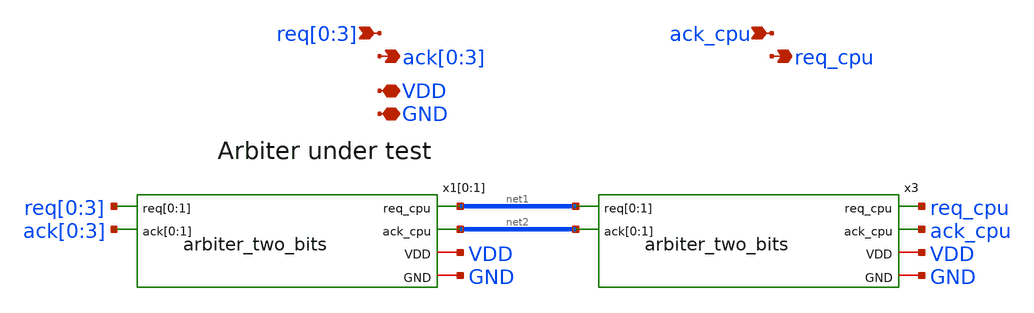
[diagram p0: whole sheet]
** sch_path: design/xschem/arbiter_tree_four_bits.sch
**.subckt arbiter_tree_four_bits req[0],req[1],req[2],req[3] ack[0],ack[1],ack[2],ack[3] ack_cpu
*+ req_cpu VDD GND
*.ipin req[0],req[1],req[2],req[3]
*.opin ack[0],ack[1],ack[2],ack[3]
*.ipin ack_cpu
*.opin req_cpu
*.iopin VDD
*.iopin GND
x3 net1[1] net1[0] ack_cpu net2[1] net2[0] req_cpu VDD GND arbiter_two_bits
x1[0] req[0] req[1] net2[1] ack[0] ack[1] net1[1] VDD GND arbiter_two_bits
x1[1] req[2] req[3] net2[0] ack[2] ack[3] net1[0] VDD GND arbiter_two_bits
**.ends

* expanding   symbol:  arbiter_two_bits.sym # of pins=6
** sym_path: design/xschem/arbiter_two_bits.sym
** sch_path: design/xschem/arbiter_two_bits.sch
.subckt arbiter_two_bits req[0] req[1] ack_cpu ack[0] ack[1] req_cpu VDD GND
*.ipin req[0],req[1]
*.opin ack[0],ack[1]
*.ipin ack_cpu
*.opin req_cpu
*.iopin VDD
*.iopin GND
x1 ack[1] ack[0] ack_cpu req_cpu req[0] req[1] VDD GND arbiter_cell_two_bits_fc
.ends


* expanding   symbol:  arbiter_cell_two_bits_fc.sym # of pins=8
** sym_path: design/xschem/arbiter_cell_two_bits_fc.sym
** sch_path: design/xschem/arbiter_cell_two_bits_fc.sch
.subckt arbiter_cell_two_bits_fc g1 g0 gc rc r0 r1 VDD GND
*.ipin r1
*.ipin r0
*.opin g0
*.opin g1
*.opin rc
*.ipin gc
*.iopin GND
*.iopin VDD
x1 net6 net5 GND GND VDD VDD net7 sky130_fd_sc_hd__nand2_1
x2 r0 gc GND GND VDD VDD net4 sky130_fd_sc_hd__or2_1
x3 net3 net1 GND GND VDD VDD g0 sky130_fd_sc_hd__nor2_1
x4 net6 net6 net6 net6 GND GND VDD VDD net3 sky130_fd_sc_hd__or4_1
x5 gc GND GND VDD VDD net1 sky130_fd_sc_hd__inv_1
x6 gc r1 GND GND VDD VDD net5 sky130_fd_sc_hd__or2_1
x7 net4 net7 GND GND VDD VDD net6 sky130_fd_sc_hd__nand2_1
x8 net7 net7 net7 net7 GND GND VDD VDD net2 sky130_fd_sc_hd__or4_1
x9 net1 net2 GND GND VDD VDD g1 sky130_fd_sc_hd__nor2_1
x10 net2 r0 GND GND VDD VDD net8 sky130_fd_sc_hd__nand2_1
x11 net3 r1 GND GND VDD VDD net9 sky130_fd_sc_hd__nand2_1
x12 net8 net9 GND GND VDD VDD rc sky130_fd_sc_hd__nand2_1
.ends

.end
